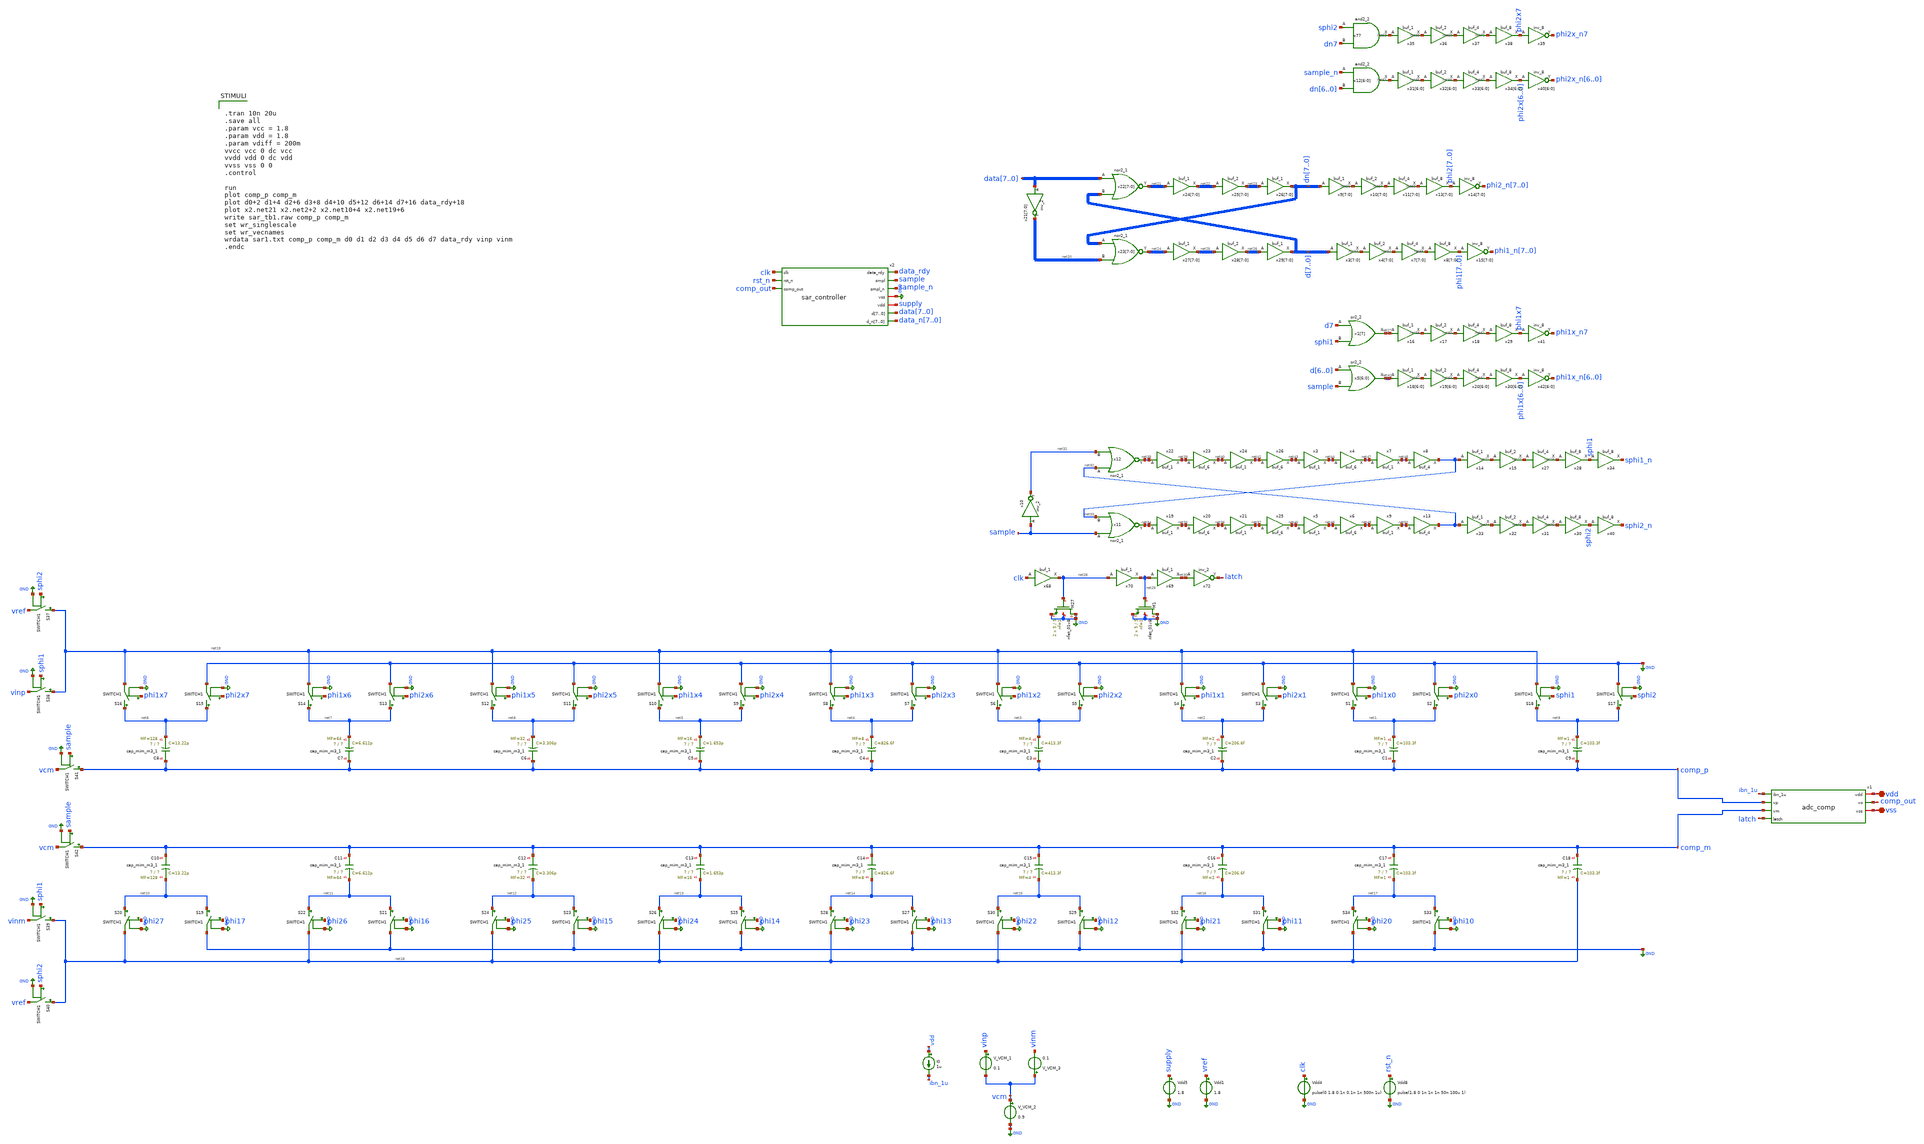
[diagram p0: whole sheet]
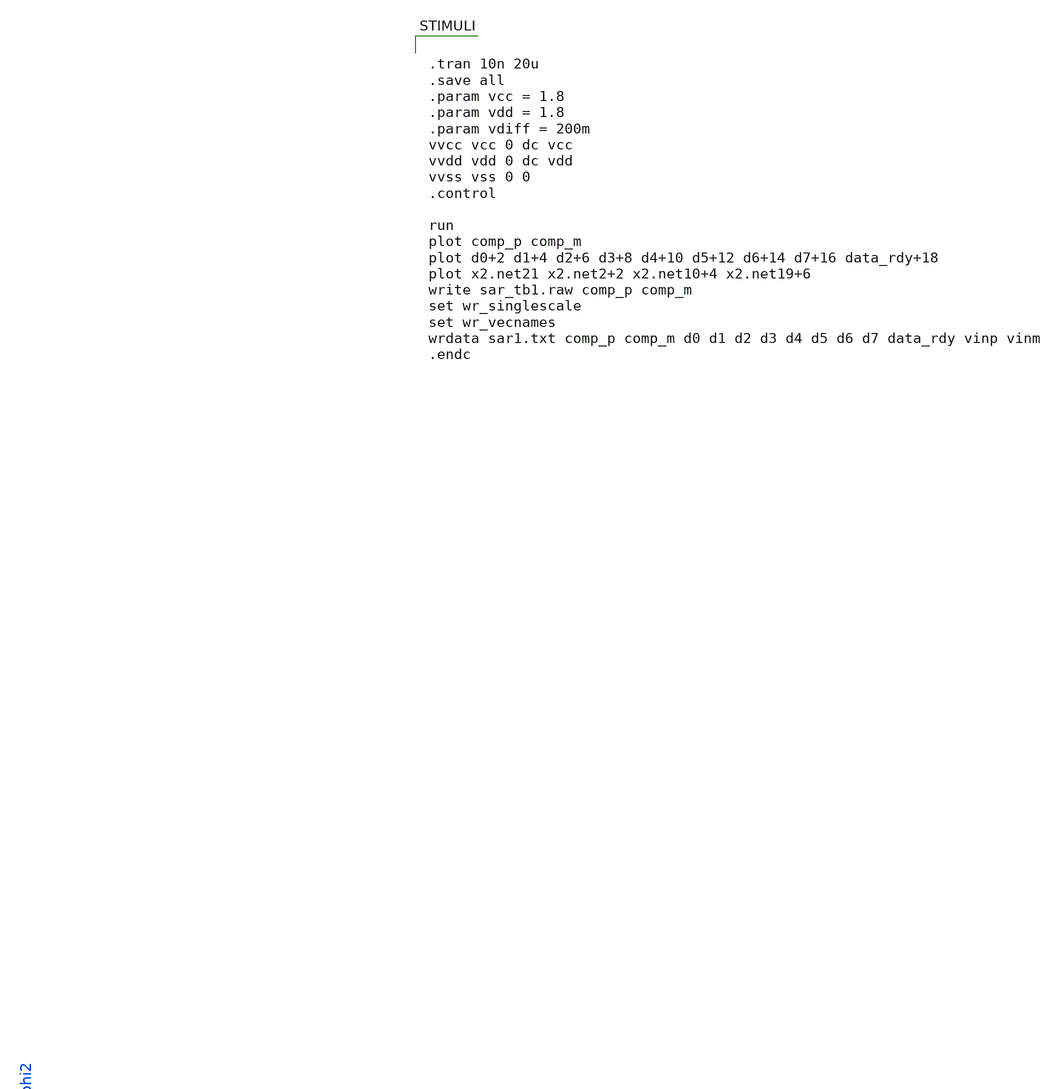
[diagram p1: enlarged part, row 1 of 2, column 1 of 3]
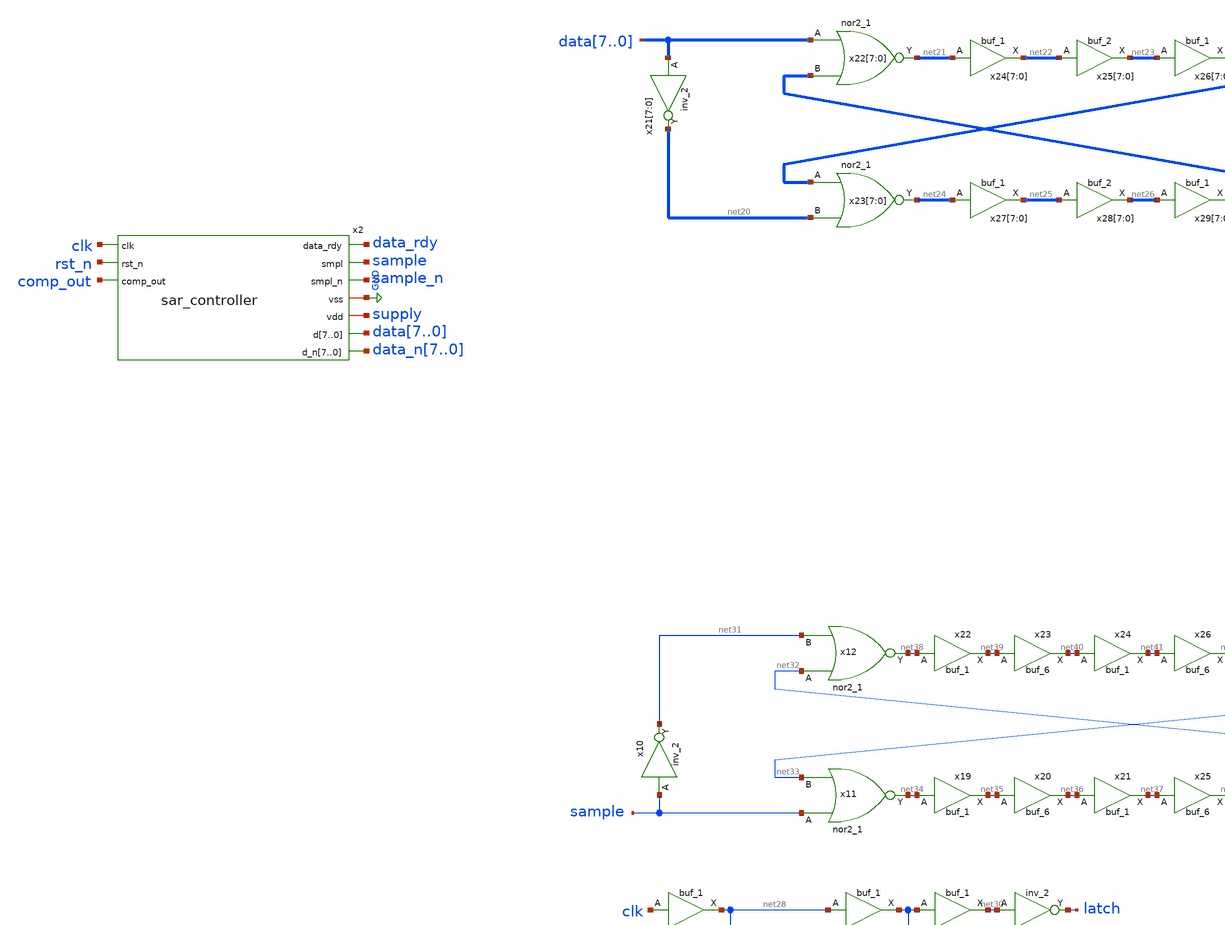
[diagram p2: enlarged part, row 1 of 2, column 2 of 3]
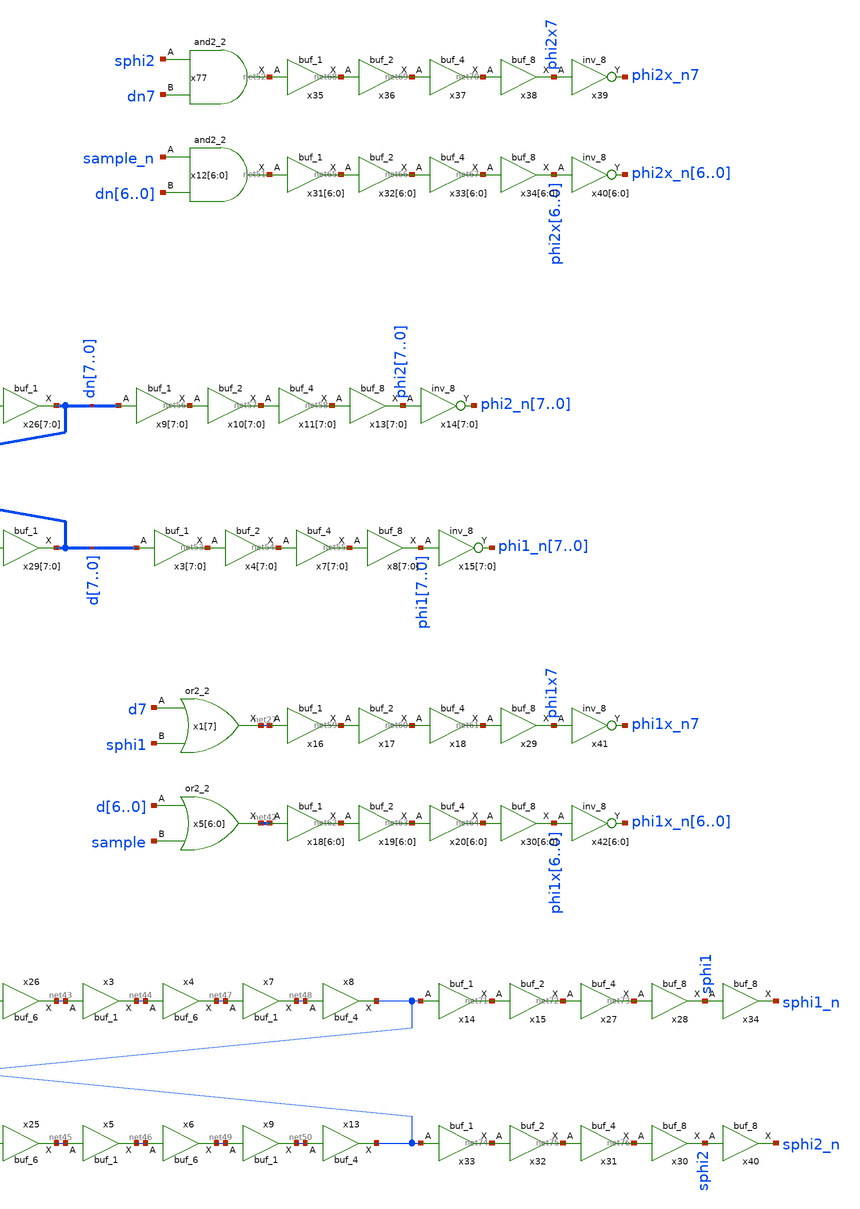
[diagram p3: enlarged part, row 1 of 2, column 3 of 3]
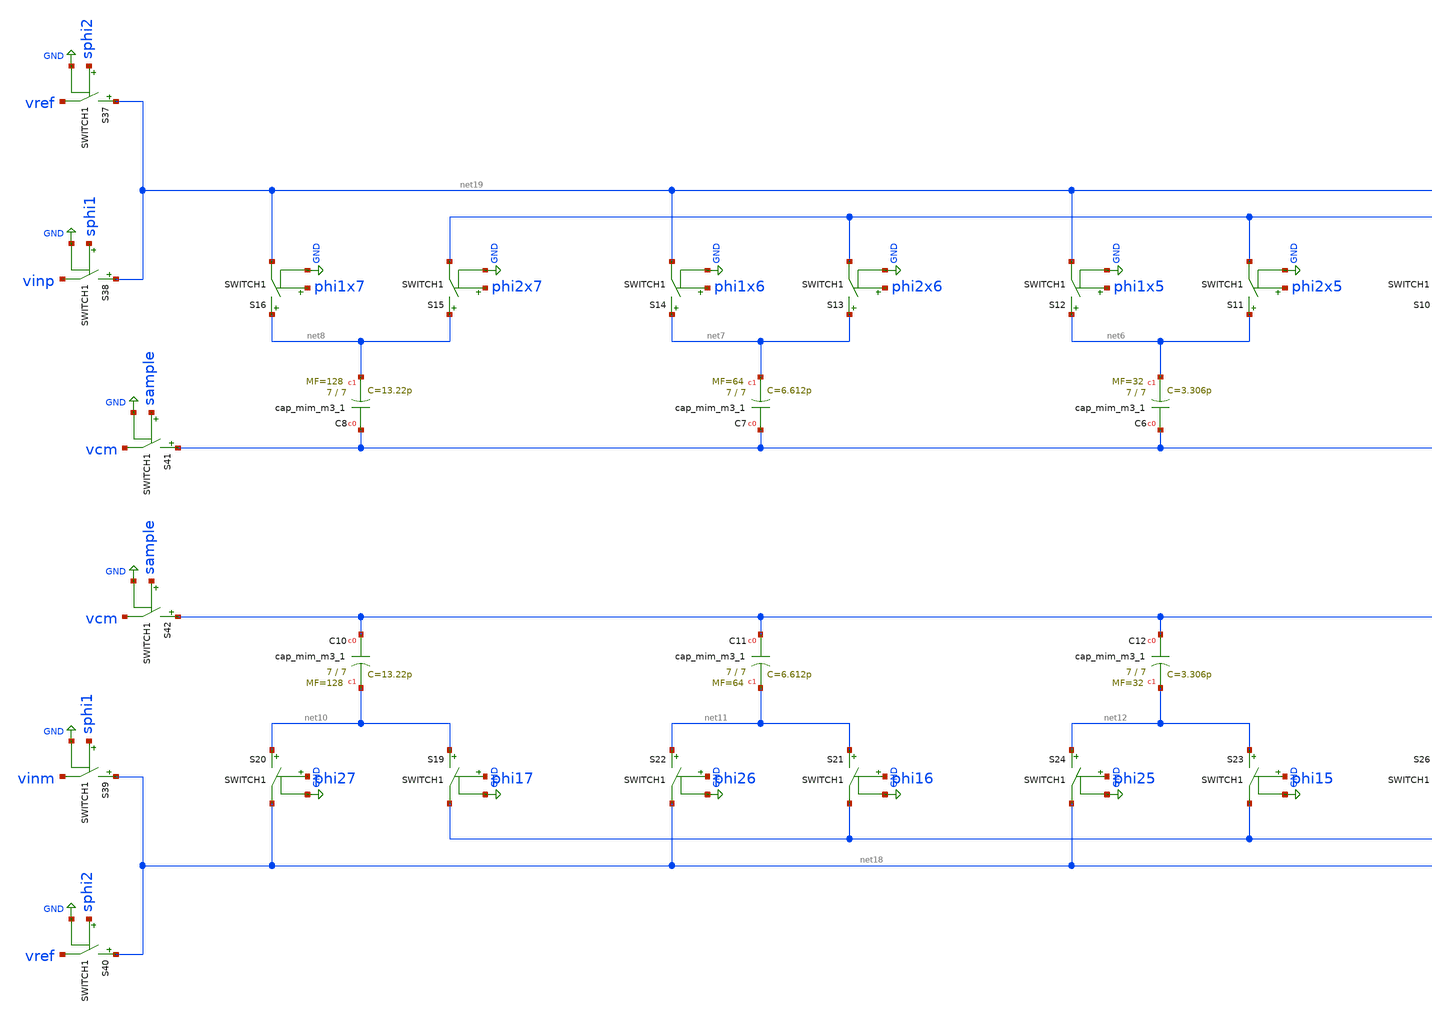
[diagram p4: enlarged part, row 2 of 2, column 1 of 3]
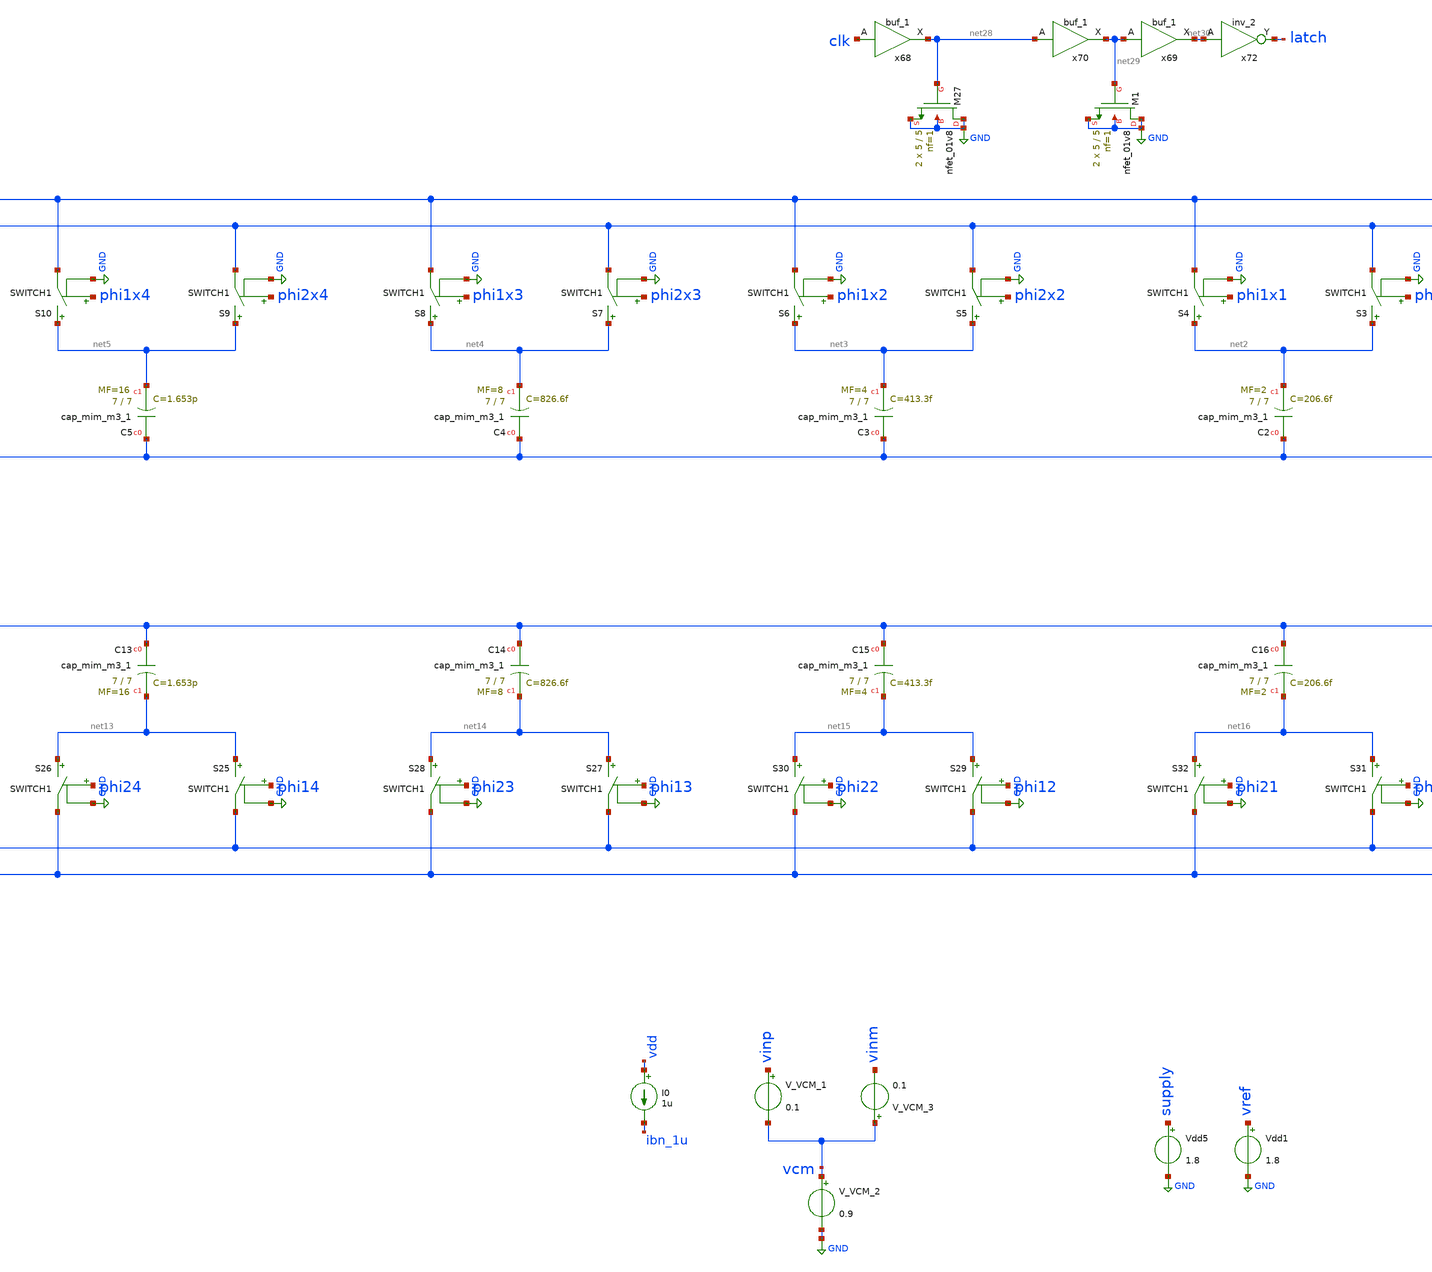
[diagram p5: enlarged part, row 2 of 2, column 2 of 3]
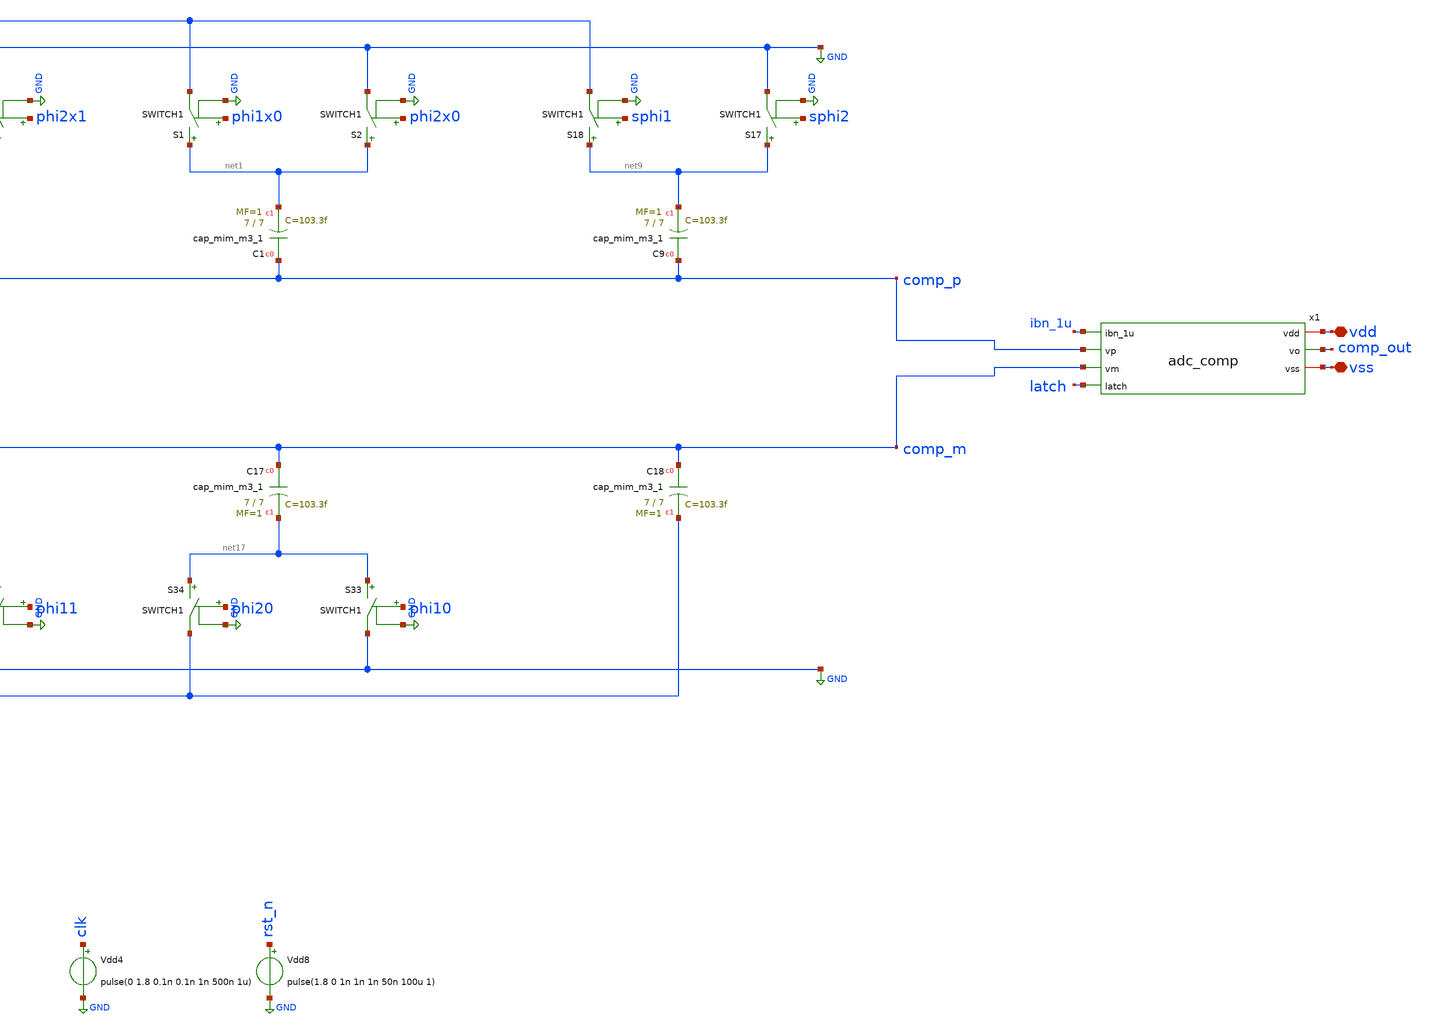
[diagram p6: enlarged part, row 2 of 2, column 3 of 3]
** sch_path: top/test/testbench/sar_tb1.sch
.lib $::SKYWATER_MODELS/sky130.lib.spice tt
.include $::SKYWATER_STDCELLS/sky130_fd_sc_hd.spice

**.subckt sar_tb1 vdd vss
*.iopin vdd
*.iopin vss
XC1 comp_p net1 sky130_fd_pr__cap_mim_m3_1 W=7 L=7 MF=1 m=1
S2 net1 GND phi2x0 GND SWITCH1
S1 net1 net19 phi1x0 GND SWITCH1
XC2 comp_p net2 sky130_fd_pr__cap_mim_m3_1 W=7 L=7 MF=2 m=2
S3 net2 GND phi2x1 GND SWITCH1
S4 net2 net19 phi1x1 GND SWITCH1
XC3 comp_p net3 sky130_fd_pr__cap_mim_m3_1 W=7 L=7 MF=4 m=4
S5 net3 GND phi2x2 GND SWITCH1
S6 net3 net19 phi1x2 GND SWITCH1
XC4 comp_p net4 sky130_fd_pr__cap_mim_m3_1 W=7 L=7 MF=8 m=8
S7 net4 GND phi2x3 GND SWITCH1
S8 net4 net19 phi1x3 GND SWITCH1
XC5 comp_p net5 sky130_fd_pr__cap_mim_m3_1 W=7 L=7 MF=16 m=16
S9 net5 GND phi2x4 GND SWITCH1
S10 net5 net19 phi1x4 GND SWITCH1
XC6 comp_p net6 sky130_fd_pr__cap_mim_m3_1 W=7 L=7 MF=32 m=32
S11 net6 GND phi2x5 GND SWITCH1
S12 net6 net19 phi1x5 GND SWITCH1
XC7 comp_p net7 sky130_fd_pr__cap_mim_m3_1 W=7 L=7 MF=64 m=64
S13 net7 GND phi2x6 GND SWITCH1
S14 net7 net19 phi1x6 GND SWITCH1
S15 net8 GND phi2x7 GND SWITCH1
S16 net8 net19 phi1x7 GND SWITCH1
XC9 comp_p net9 sky130_fd_pr__cap_mim_m3_1 W=7 L=7 MF=1 m=1
S17 net9 GND sphi2 GND SWITCH1
S18 net9 net19 sphi1 GND SWITCH1
XC10 comp_m net10 sky130_fd_pr__cap_mim_m3_1 W=7 L=7 MF=128 m=128
S19 net10 GND phi17 GND SWITCH1
S20 net10 net18 phi27 GND SWITCH1
XC11 comp_m net11 sky130_fd_pr__cap_mim_m3_1 W=7 L=7 MF=64 m=64
S21 net11 GND phi16 GND SWITCH1
S22 net11 net18 phi26 GND SWITCH1
XC12 comp_m net12 sky130_fd_pr__cap_mim_m3_1 W=7 L=7 MF=32 m=32
S23 net12 GND phi15 GND SWITCH1
S24 net12 net18 phi25 GND SWITCH1
XC13 comp_m net13 sky130_fd_pr__cap_mim_m3_1 W=7 L=7 MF=16 m=16
S25 net13 GND phi14 GND SWITCH1
S26 net13 net18 phi24 GND SWITCH1
XC14 comp_m net14 sky130_fd_pr__cap_mim_m3_1 W=7 L=7 MF=8 m=8
S27 net14 GND phi13 GND SWITCH1
S28 net14 net18 phi23 GND SWITCH1
XC15 comp_m net15 sky130_fd_pr__cap_mim_m3_1 W=7 L=7 MF=4 m=4
S29 net15 GND phi12 GND SWITCH1
S30 net15 net18 phi22 GND SWITCH1
XC16 comp_m net16 sky130_fd_pr__cap_mim_m3_1 W=7 L=7 MF=2 m=2
S31 net16 GND phi11 GND SWITCH1
S32 net16 net18 phi21 GND SWITCH1
XC17 comp_m net17 sky130_fd_pr__cap_mim_m3_1 W=7 L=7 MF=1 m=1
S33 net17 GND phi10 GND SWITCH1
S34 net17 net18 phi20 GND SWITCH1
XC18 comp_m net18 sky130_fd_pr__cap_mim_m3_1 W=7 L=7 MF=1 m=1
S37 net19 vref sphi2 GND SWITCH1
S39 net18 vinm sphi1 GND SWITCH1
S40 net18 vref sphi2 GND SWITCH1
S41 comp_p vcm sample GND SWITCH1
S42 comp_m vcm sample GND SWITCH1
Vdd8 rst_n GND pulse(1.8 0 1n 1n 1n 50n 100u 1)
Vdd4 clk GND pulse(0 1.8 0.1n 0.1n 1n 500n 1u)
Vdd1 vref GND 1.8
S38 net19 vinp sphi1 GND SWITCH1
XC8 comp_p net8 sky130_fd_pr__cap_mim_m3_1 W=7 L=7 MF=128 m=128
x2 clk data_rdy sample rst_n sample_n comp_out GND supply data7 data6 data5 data4 data3 data2 data1
+ data0 data_n7 data_n6 data_n5 data_n4 data_n3 data_n2 data_n1 data_n0 sar_controller
Vdd5 supply GND 1.8
V_VCM_2 vcm GND 0.9
V_VCM_1 vinp vcm 0.1
V_VCM_3 vcm vinm 0.1
x21[7] data7 vss vss vcc vcc net20[7] sky130_fd_sc_hd__inv_2
x21[6] data6 vss vss vcc vcc net20[6] sky130_fd_sc_hd__inv_2
x21[5] data5 vss vss vcc vcc net20[5] sky130_fd_sc_hd__inv_2
x21[4] data4 vss vss vcc vcc net20[4] sky130_fd_sc_hd__inv_2
x21[3] data3 vss vss vcc vcc net20[3] sky130_fd_sc_hd__inv_2
x21[2] data2 vss vss vcc vcc net20[2] sky130_fd_sc_hd__inv_2
x21[1] data1 vss vss vcc vcc net20[1] sky130_fd_sc_hd__inv_2
x21[0] data0 vss vss vcc vcc net20[0] sky130_fd_sc_hd__inv_2
x22[7] data7 d7 vss vss vdd vdd net21[7] sky130_fd_sc_hd__nor2_1
x22[6] data6 d6 vss vss vdd vdd net21[6] sky130_fd_sc_hd__nor2_1
x22[5] data5 d5 vss vss vdd vdd net21[5] sky130_fd_sc_hd__nor2_1
x22[4] data4 d4 vss vss vdd vdd net21[4] sky130_fd_sc_hd__nor2_1
x22[3] data3 d3 vss vss vdd vdd net21[3] sky130_fd_sc_hd__nor2_1
x22[2] data2 d2 vss vss vdd vdd net21[2] sky130_fd_sc_hd__nor2_1
x22[1] data1 d1 vss vss vdd vdd net21[1] sky130_fd_sc_hd__nor2_1
x22[0] data0 d0 vss vss vdd vdd net21[0] sky130_fd_sc_hd__nor2_1
x23[7] dn7 net20[7] vss vss vdd vdd net24[7] sky130_fd_sc_hd__nor2_1
x23[6] dn6 net20[6] vss vss vdd vdd net24[6] sky130_fd_sc_hd__nor2_1
x23[5] dn5 net20[5] vss vss vdd vdd net24[5] sky130_fd_sc_hd__nor2_1
x23[4] dn4 net20[4] vss vss vdd vdd net24[4] sky130_fd_sc_hd__nor2_1
x23[3] dn3 net20[3] vss vss vdd vdd net24[3] sky130_fd_sc_hd__nor2_1
x23[2] dn2 net20[2] vss vss vdd vdd net24[2] sky130_fd_sc_hd__nor2_1
x23[1] dn1 net20[1] vss vss vdd vdd net24[1] sky130_fd_sc_hd__nor2_1
x23[0] dn0 net20[0] vss vss vdd vdd net24[0] sky130_fd_sc_hd__nor2_1
x24[7] net21[7] vss vss vdd vdd net22[7] sky130_fd_sc_hd__buf_1
x24[6] net21[6] vss vss vdd vdd net22[6] sky130_fd_sc_hd__buf_1
x24[5] net21[5] vss vss vdd vdd net22[5] sky130_fd_sc_hd__buf_1
x24[4] net21[4] vss vss vdd vdd net22[4] sky130_fd_sc_hd__buf_1
x24[3] net21[3] vss vss vdd vdd net22[3] sky130_fd_sc_hd__buf_1
x24[2] net21[2] vss vss vdd vdd net22[2] sky130_fd_sc_hd__buf_1
x24[1] net21[1] vss vss vdd vdd net22[1] sky130_fd_sc_hd__buf_1
x24[0] net21[0] vss vss vdd vdd net22[0] sky130_fd_sc_hd__buf_1
x25[7] net22[7] vss vss vdd vdd net23[7] sky130_fd_sc_hd__buf_2
x25[6] net22[6] vss vss vdd vdd net23[6] sky130_fd_sc_hd__buf_2
x25[5] net22[5] vss vss vdd vdd net23[5] sky130_fd_sc_hd__buf_2
x25[4] net22[4] vss vss vdd vdd net23[4] sky130_fd_sc_hd__buf_2
x25[3] net22[3] vss vss vdd vdd net23[3] sky130_fd_sc_hd__buf_2
x25[2] net22[2] vss vss vdd vdd net23[2] sky130_fd_sc_hd__buf_2
x25[1] net22[1] vss vss vdd vdd net23[1] sky130_fd_sc_hd__buf_2
x25[0] net22[0] vss vss vdd vdd net23[0] sky130_fd_sc_hd__buf_2
x26[7] net23[7] vss vss vdd vdd dn7 sky130_fd_sc_hd__buf_1
x26[6] net23[6] vss vss vdd vdd dn6 sky130_fd_sc_hd__buf_1
x26[5] net23[5] vss vss vdd vdd dn5 sky130_fd_sc_hd__buf_1
x26[4] net23[4] vss vss vdd vdd dn4 sky130_fd_sc_hd__buf_1
x26[3] net23[3] vss vss vdd vdd dn3 sky130_fd_sc_hd__buf_1
x26[2] net23[2] vss vss vdd vdd dn2 sky130_fd_sc_hd__buf_1
x26[1] net23[1] vss vss vdd vdd dn1 sky130_fd_sc_hd__buf_1
x26[0] net23[0] vss vss vdd vdd dn0 sky130_fd_sc_hd__buf_1
x27[7] net24[7] vss vss vdd vdd net25[7] sky130_fd_sc_hd__buf_1
x27[6] net24[6] vss vss vdd vdd net25[6] sky130_fd_sc_hd__buf_1
x27[5] net24[5] vss vss vdd vdd net25[5] sky130_fd_sc_hd__buf_1
x27[4] net24[4] vss vss vdd vdd net25[4] sky130_fd_sc_hd__buf_1
x27[3] net24[3] vss vss vdd vdd net25[3] sky130_fd_sc_hd__buf_1
x27[2] net24[2] vss vss vdd vdd net25[2] sky130_fd_sc_hd__buf_1
x27[1] net24[1] vss vss vdd vdd net25[1] sky130_fd_sc_hd__buf_1
x27[0] net24[0] vss vss vdd vdd net25[0] sky130_fd_sc_hd__buf_1
x28[7] net25[7] vss vss vdd vdd net26[7] sky130_fd_sc_hd__buf_2
x28[6] net25[6] vss vss vdd vdd net26[6] sky130_fd_sc_hd__buf_2
x28[5] net25[5] vss vss vdd vdd net26[5] sky130_fd_sc_hd__buf_2
x28[4] net25[4] vss vss vdd vdd net26[4] sky130_fd_sc_hd__buf_2
x28[3] net25[3] vss vss vdd vdd net26[3] sky130_fd_sc_hd__buf_2
x28[2] net25[2] vss vss vdd vdd net26[2] sky130_fd_sc_hd__buf_2
x28[1] net25[1] vss vss vdd vdd net26[1] sky130_fd_sc_hd__buf_2
x28[0] net25[0] vss vss vdd vdd net26[0] sky130_fd_sc_hd__buf_2
x29[7] net26[7] vss vss vdd vdd d7 sky130_fd_sc_hd__buf_1
x29[6] net26[6] vss vss vdd vdd d6 sky130_fd_sc_hd__buf_1
x29[5] net26[5] vss vss vdd vdd d5 sky130_fd_sc_hd__buf_1
x29[4] net26[4] vss vss vdd vdd d4 sky130_fd_sc_hd__buf_1
x29[3] net26[3] vss vss vdd vdd d3 sky130_fd_sc_hd__buf_1
x29[2] net26[2] vss vss vdd vdd d2 sky130_fd_sc_hd__buf_1
x29[1] net26[1] vss vss vdd vdd d1 sky130_fd_sc_hd__buf_1
x29[0] net26[0] vss vss vdd vdd d0 sky130_fd_sc_hd__buf_1
x1[7] d7 sphi1 vss vss vcc vcc net27 sky130_fd_sc_hd__or2_2
x12[6] sample_n dn6 vss vss vcc vcc net51[6] sky130_fd_sc_hd__and2_2
x12[5] sample_n dn5 vss vss vcc vcc net51[5] sky130_fd_sc_hd__and2_2
x12[4] sample_n dn4 vss vss vcc vcc net51[4] sky130_fd_sc_hd__and2_2
x12[3] sample_n dn3 vss vss vcc vcc net51[3] sky130_fd_sc_hd__and2_2
x12[2] sample_n dn2 vss vss vcc vcc net51[2] sky130_fd_sc_hd__and2_2
x12[1] sample_n dn1 vss vss vcc vcc net51[1] sky130_fd_sc_hd__and2_2
x12[0] sample_n dn0 vss vss vcc vcc net51[0] sky130_fd_sc_hd__and2_2
x1 vdd comp_out ibn_1u comp_p comp_m vss latch adc_comp
I0 vdd ibn_1u 1u
x68 clk vss vss vdd vdd net28 sky130_fd_sc_hd__buf_1
x70 net28 vss vss vdd vdd net29 sky130_fd_sc_hd__buf_1
x72 net30 vss vss vcc vcc latch sky130_fd_sc_hd__inv_2
XM27 GND net28 GND GND sky130_fd_pr__nfet_01v8 L=5 W=5 nf=1 ad='int((nf+1)/2) * W/nf * 0.29' as='int((nf+2)/2) * W/nf * 0.29'
+ pd='2*int((nf+1)/2) * (W/nf + 0.29)' ps='2*int((nf+2)/2) * (W/nf + 0.29)' nrd='0.29 / W' nrs='0.29 / W'
+ sa=0 sb=0 sd=0 mult=2 m=2
XM1 GND net29 GND GND sky130_fd_pr__nfet_01v8 L=5 W=5 nf=1 ad='int((nf+1)/2) * W/nf * 0.29' as='int((nf+2)/2) * W/nf * 0.29'
+ pd='2*int((nf+1)/2) * (W/nf + 0.29)' ps='2*int((nf+2)/2) * (W/nf + 0.29)' nrd='0.29 / W' nrs='0.29 / W'
+ sa=0 sb=0 sd=0 mult=2 m=2
x69 net29 vss vss vdd vdd net30 sky130_fd_sc_hd__buf_1
x10 sample vss vss vcc vcc net31 sky130_fd_sc_hd__inv_2
x11 sample net33 vss vss vdd vdd net34 sky130_fd_sc_hd__nor2_1
x12 net32 net31 vss vss vdd vdd net38 sky130_fd_sc_hd__nor2_1
x19 net34 vss vss vdd vdd net35 sky130_fd_sc_hd__buf_1
x20 net35 vss vss vdd vdd net36 sky130_fd_sc_hd__buf_6
x21 net36 vss vss vdd vdd net37 sky130_fd_sc_hd__buf_1
x22 net38 vss vss vdd vdd net39 sky130_fd_sc_hd__buf_1
x23 net39 vss vss vdd vdd net40 sky130_fd_sc_hd__buf_6
x24 net40 vss vss vdd vdd net41 sky130_fd_sc_hd__buf_1
x25 net37 vss vss vdd vdd net45 sky130_fd_sc_hd__buf_6
x26 net41 vss vss vdd vdd net43 sky130_fd_sc_hd__buf_6
x5[6] d6 sample vss vss vcc vcc net42[6] sky130_fd_sc_hd__or2_2
x5[5] d5 sample vss vss vcc vcc net42[5] sky130_fd_sc_hd__or2_2
x5[4] d4 sample vss vss vcc vcc net42[4] sky130_fd_sc_hd__or2_2
x5[3] d3 sample vss vss vcc vcc net42[3] sky130_fd_sc_hd__or2_2
x5[2] d2 sample vss vss vcc vcc net42[2] sky130_fd_sc_hd__or2_2
x5[1] d1 sample vss vss vcc vcc net42[1] sky130_fd_sc_hd__or2_2
x5[0] d0 sample vss vss vcc vcc net42[0] sky130_fd_sc_hd__or2_2
x77 sphi2 dn7 vss vss vcc vcc net52 sky130_fd_sc_hd__and2_2
x3 net43 vss vss vdd vdd net44 sky130_fd_sc_hd__buf_1
x4 net44 vss vss vdd vdd net47 sky130_fd_sc_hd__buf_6
x5 net45 vss vss vdd vdd net46 sky130_fd_sc_hd__buf_1
x6 net46 vss vss vdd vdd net49 sky130_fd_sc_hd__buf_6
x7 net47 vss vss vdd vdd net48 sky130_fd_sc_hd__buf_1
x8 net48 vss vss vdd vdd net33 sky130_fd_sc_hd__buf_4
x9 net49 vss vss vdd vdd net50 sky130_fd_sc_hd__buf_1
x13 net50 vss vss vdd vdd net32 sky130_fd_sc_hd__buf_4
x3[7] d7 vss vss vdd vdd net53[7] sky130_fd_sc_hd__buf_1
x3[6] d6 vss vss vdd vdd net53[6] sky130_fd_sc_hd__buf_1
x3[5] d5 vss vss vdd vdd net53[5] sky130_fd_sc_hd__buf_1
x3[4] d4 vss vss vdd vdd net53[4] sky130_fd_sc_hd__buf_1
x3[3] d3 vss vss vdd vdd net53[3] sky130_fd_sc_hd__buf_1
x3[2] d2 vss vss vdd vdd net53[2] sky130_fd_sc_hd__buf_1
x3[1] d1 vss vss vdd vdd net53[1] sky130_fd_sc_hd__buf_1
x3[0] d0 vss vss vdd vdd net53[0] sky130_fd_sc_hd__buf_1
x4[7] net53[7] vss vss vdd vdd net54[7] sky130_fd_sc_hd__buf_2
x4[6] net53[6] vss vss vdd vdd net54[6] sky130_fd_sc_hd__buf_2
x4[5] net53[5] vss vss vdd vdd net54[5] sky130_fd_sc_hd__buf_2
x4[4] net53[4] vss vss vdd vdd net54[4] sky130_fd_sc_hd__buf_2
x4[3] net53[3] vss vss vdd vdd net54[3] sky130_fd_sc_hd__buf_2
x4[2] net53[2] vss vss vdd vdd net54[2] sky130_fd_sc_hd__buf_2
x4[1] net53[1] vss vss vdd vdd net54[1] sky130_fd_sc_hd__buf_2
x4[0] net53[0] vss vss vdd vdd net54[0] sky130_fd_sc_hd__buf_2
x7[7] net54[7] vss vss vdd vdd net55[7] sky130_fd_sc_hd__buf_4
x7[6] net54[6] vss vss vdd vdd net55[6] sky130_fd_sc_hd__buf_4
x7[5] net54[5] vss vss vdd vdd net55[5] sky130_fd_sc_hd__buf_4
x7[4] net54[4] vss vss vdd vdd net55[4] sky130_fd_sc_hd__buf_4
x7[3] net54[3] vss vss vdd vdd net55[3] sky130_fd_sc_hd__buf_4
x7[2] net54[2] vss vss vdd vdd net55[2] sky130_fd_sc_hd__buf_4
x7[1] net54[1] vss vss vdd vdd net55[1] sky130_fd_sc_hd__buf_4
x7[0] net54[0] vss vss vdd vdd net55[0] sky130_fd_sc_hd__buf_4
x8[7] net55[7] vss vss vdd vdd phi17 sky130_fd_sc_hd__buf_8
x8[6] net55[6] vss vss vdd vdd phi16 sky130_fd_sc_hd__buf_8
x8[5] net55[5] vss vss vdd vdd phi15 sky130_fd_sc_hd__buf_8
x8[4] net55[4] vss vss vdd vdd phi14 sky130_fd_sc_hd__buf_8
x8[3] net55[3] vss vss vdd vdd phi13 sky130_fd_sc_hd__buf_8
x8[2] net55[2] vss vss vdd vdd phi12 sky130_fd_sc_hd__buf_8
x8[1] net55[1] vss vss vdd vdd phi11 sky130_fd_sc_hd__buf_8
x8[0] net55[0] vss vss vdd vdd phi10 sky130_fd_sc_hd__buf_8
x9[7] dn7 vss vss vdd vdd net56[7] sky130_fd_sc_hd__buf_1
x9[6] dn6 vss vss vdd vdd net56[6] sky130_fd_sc_hd__buf_1
x9[5] dn5 vss vss vdd vdd net56[5] sky130_fd_sc_hd__buf_1
x9[4] dn4 vss vss vdd vdd net56[4] sky130_fd_sc_hd__buf_1
x9[3] dn3 vss vss vdd vdd net56[3] sky130_fd_sc_hd__buf_1
x9[2] dn2 vss vss vdd vdd net56[2] sky130_fd_sc_hd__buf_1
x9[1] dn1 vss vss vdd vdd net56[1] sky130_fd_sc_hd__buf_1
x9[0] dn0 vss vss vdd vdd net56[0] sky130_fd_sc_hd__buf_1
x10[7] net56[7] vss vss vdd vdd net57[7] sky130_fd_sc_hd__buf_2
x10[6] net56[6] vss vss vdd vdd net57[6] sky130_fd_sc_hd__buf_2
x10[5] net56[5] vss vss vdd vdd net57[5] sky130_fd_sc_hd__buf_2
x10[4] net56[4] vss vss vdd vdd net57[4] sky130_fd_sc_hd__buf_2
x10[3] net56[3] vss vss vdd vdd net57[3] sky130_fd_sc_hd__buf_2
x10[2] net56[2] vss vss vdd vdd net57[2] sky130_fd_sc_hd__buf_2
x10[1] net56[1] vss vss vdd vdd net57[1] sky130_fd_sc_hd__buf_2
x10[0] net56[0] vss vss vdd vdd net57[0] sky130_fd_sc_hd__buf_2
x11[7] net57[7] vss vss vdd vdd net58[7] sky130_fd_sc_hd__buf_4
x11[6] net57[6] vss vss vdd vdd net58[6] sky130_fd_sc_hd__buf_4
x11[5] net57[5] vss vss vdd vdd net58[5] sky130_fd_sc_hd__buf_4
x11[4] net57[4] vss vss vdd vdd net58[4] sky130_fd_sc_hd__buf_4
x11[3] net57[3] vss vss vdd vdd net58[3] sky130_fd_sc_hd__buf_4
x11[2] net57[2] vss vss vdd vdd net58[2] sky130_fd_sc_hd__buf_4
x11[1] net57[1] vss vss vdd vdd net58[1] sky130_fd_sc_hd__buf_4
x11[0] net57[0] vss vss vdd vdd net58[0] sky130_fd_sc_hd__buf_4
x13[7] net58[7] vss vss vdd vdd phi27 sky130_fd_sc_hd__buf_8
x13[6] net58[6] vss vss vdd vdd phi26 sky130_fd_sc_hd__buf_8
x13[5] net58[5] vss vss vdd vdd phi25 sky130_fd_sc_hd__buf_8
x13[4] net58[4] vss vss vdd vdd phi24 sky130_fd_sc_hd__buf_8
x13[3] net58[3] vss vss vdd vdd phi23 sky130_fd_sc_hd__buf_8
x13[2] net58[2] vss vss vdd vdd phi22 sky130_fd_sc_hd__buf_8
x13[1] net58[1] vss vss vdd vdd phi21 sky130_fd_sc_hd__buf_8
x13[0] net58[0] vss vss vdd vdd phi20 sky130_fd_sc_hd__buf_8
x14[7] phi27 vss vss vdd vdd phi2_n7 sky130_fd_sc_hd__inv_8
x14[6] phi26 vss vss vdd vdd phi2_n6 sky130_fd_sc_hd__inv_8
x14[5] phi25 vss vss vdd vdd phi2_n5 sky130_fd_sc_hd__inv_8
x14[4] phi24 vss vss vdd vdd phi2_n4 sky130_fd_sc_hd__inv_8
x14[3] phi23 vss vss vdd vdd phi2_n3 sky130_fd_sc_hd__inv_8
x14[2] phi22 vss vss vdd vdd phi2_n2 sky130_fd_sc_hd__inv_8
x14[1] phi21 vss vss vdd vdd phi2_n1 sky130_fd_sc_hd__inv_8
x14[0] phi20 vss vss vdd vdd phi2_n0 sky130_fd_sc_hd__inv_8
x15[7] phi17 vss vss vdd vdd phi1_n7 sky130_fd_sc_hd__inv_8
x15[6] phi16 vss vss vdd vdd phi1_n6 sky130_fd_sc_hd__inv_8
x15[5] phi15 vss vss vdd vdd phi1_n5 sky130_fd_sc_hd__inv_8
x15[4] phi14 vss vss vdd vdd phi1_n4 sky130_fd_sc_hd__inv_8
x15[3] phi13 vss vss vdd vdd phi1_n3 sky130_fd_sc_hd__inv_8
x15[2] phi12 vss vss vdd vdd phi1_n2 sky130_fd_sc_hd__inv_8
x15[1] phi11 vss vss vdd vdd phi1_n1 sky130_fd_sc_hd__inv_8
x15[0] phi10 vss vss vdd vdd phi1_n0 sky130_fd_sc_hd__inv_8
x16 net27 vss vss vdd vdd net59 sky130_fd_sc_hd__buf_1
x17 net59 vss vss vdd vdd net60 sky130_fd_sc_hd__buf_2
x18 net60 vss vss vdd vdd net61 sky130_fd_sc_hd__buf_4
x29 net61 vss vss vdd vdd phi1x7 sky130_fd_sc_hd__buf_8
x18[6] net42[6] vss vss vdd vdd net62[6] sky130_fd_sc_hd__buf_1
x18[5] net42[5] vss vss vdd vdd net62[5] sky130_fd_sc_hd__buf_1
x18[4] net42[4] vss vss vdd vdd net62[4] sky130_fd_sc_hd__buf_1
x18[3] net42[3] vss vss vdd vdd net62[3] sky130_fd_sc_hd__buf_1
x18[2] net42[2] vss vss vdd vdd net62[2] sky130_fd_sc_hd__buf_1
x18[1] net42[1] vss vss vdd vdd net62[1] sky130_fd_sc_hd__buf_1
x18[0] net42[0] vss vss vdd vdd net62[0] sky130_fd_sc_hd__buf_1
x19[6] net62[6] vss vss vdd vdd net63[6] sky130_fd_sc_hd__buf_2
x19[5] net62[5] vss vss vdd vdd net63[5] sky130_fd_sc_hd__buf_2
x19[4] net62[4] vss vss vdd vdd net63[4] sky130_fd_sc_hd__buf_2
x19[3] net62[3] vss vss vdd vdd net63[3] sky130_fd_sc_hd__buf_2
x19[2] net62[2] vss vss vdd vdd net63[2] sky130_fd_sc_hd__buf_2
x19[1] net62[1] vss vss vdd vdd net63[1] sky130_fd_sc_hd__buf_2
x19[0] net62[0] vss vss vdd vdd net63[0] sky130_fd_sc_hd__buf_2
x20[6] net63[6] vss vss vdd vdd net64[6] sky130_fd_sc_hd__buf_4
x20[5] net63[5] vss vss vdd vdd net64[5] sky130_fd_sc_hd__buf_4
x20[4] net63[4] vss vss vdd vdd net64[4] sky130_fd_sc_hd__buf_4
x20[3] net63[3] vss vss vdd vdd net64[3] sky130_fd_sc_hd__buf_4
x20[2] net63[2] vss vss vdd vdd net64[2] sky130_fd_sc_hd__buf_4
x20[1] net63[1] vss vss vdd vdd net64[1] sky130_fd_sc_hd__buf_4
x20[0] net63[0] vss vss vdd vdd net64[0] sky130_fd_sc_hd__buf_4
x30[6] net64[6] vss vss vdd vdd phi1x6 sky130_fd_sc_hd__buf_8
x30[5] net64[5] vss vss vdd vdd phi1x5 sky130_fd_sc_hd__buf_8
x30[4] net64[4] vss vss vdd vdd phi1x4 sky130_fd_sc_hd__buf_8
x30[3] net64[3] vss vss vdd vdd phi1x3 sky130_fd_sc_hd__buf_8
x30[2] net64[2] vss vss vdd vdd phi1x2 sky130_fd_sc_hd__buf_8
x30[1] net64[1] vss vss vdd vdd phi1x1 sky130_fd_sc_hd__buf_8
x30[0] net64[0] vss vss vdd vdd phi1x0 sky130_fd_sc_hd__buf_8
x31[6] net51[6] vss vss vdd vdd net65[6] sky130_fd_sc_hd__buf_1
x31[5] net51[5] vss vss vdd vdd net65[5] sky130_fd_sc_hd__buf_1
x31[4] net51[4] vss vss vdd vdd net65[4] sky130_fd_sc_hd__buf_1
x31[3] net51[3] vss vss vdd vdd net65[3] sky130_fd_sc_hd__buf_1
x31[2] net51[2] vss vss vdd vdd net65[2] sky130_fd_sc_hd__buf_1
x31[1] net51[1] vss vss vdd vdd net65[1] sky130_fd_sc_hd__buf_1
x31[0] net51[0] vss vss vdd vdd net65[0] sky130_fd_sc_hd__buf_1
x32[6] net65[6] vss vss vdd vdd net66[6] sky130_fd_sc_hd__buf_2
x32[5] net65[5] vss vss vdd vdd net66[5] sky130_fd_sc_hd__buf_2
x32[4] net65[4] vss vss vdd vdd net66[4] sky130_fd_sc_hd__buf_2
x32[3] net65[3] vss vss vdd vdd net66[3] sky130_fd_sc_hd__buf_2
x32[2] net65[2] vss vss vdd vdd net66[2] sky130_fd_sc_hd__buf_2
x32[1] net65[1] vss vss vdd vdd net66[1] sky130_fd_sc_hd__buf_2
x32[0] net65[0] vss vss vdd vdd net66[0] sky130_fd_sc_hd__buf_2
x33[6] net66[6] vss vss vdd vdd net67[6] sky130_fd_sc_hd__buf_4
x33[5] net66[5] vss vss vdd vdd net67[5] sky130_fd_sc_hd__buf_4
x33[4] net66[4] vss vss vdd vdd net67[4] sky130_fd_sc_hd__buf_4
x33[3] net66[3] vss vss vdd vdd net67[3] sky130_fd_sc_hd__buf_4
x33[2] net66[2] vss vss vdd vdd net67[2] sky130_fd_sc_hd__buf_4
x33[1] net66[1] vss vss vdd vdd net67[1] sky130_fd_sc_hd__buf_4
x33[0] net66[0] vss vss vdd vdd net67[0] sky130_fd_sc_hd__buf_4
x34[6] net67[6] vss vss vdd vdd phi2x6 sky130_fd_sc_hd__buf_8
x34[5] net67[5] vss vss vdd vdd phi2x5 sky130_fd_sc_hd__buf_8
x34[4] net67[4] vss vss vdd vdd phi2x4 sky130_fd_sc_hd__buf_8
x34[3] net67[3] vss vss vdd vdd phi2x3 sky130_fd_sc_hd__buf_8
x34[2] net67[2] vss vss vdd vdd phi2x2 sky130_fd_sc_hd__buf_8
x34[1] net67[1] vss vss vdd vdd phi2x1 sky130_fd_sc_hd__buf_8
x34[0] net67[0] vss vss vdd vdd phi2x0 sky130_fd_sc_hd__buf_8
x35 net52 vss vss vdd vdd net68 sky130_fd_sc_hd__buf_1
x36 net68 vss vss vdd vdd net69 sky130_fd_sc_hd__buf_2
x37 net69 vss vss vdd vdd net70 sky130_fd_sc_hd__buf_4
x38 net70 vss vss vdd vdd phi2x7 sky130_fd_sc_hd__buf_8
x39 phi2x7 vss vss vdd vdd phi2x_n7 sky130_fd_sc_hd__inv_8
x40[6] phi2x6 vss vss vdd vdd phi2x_n6 sky130_fd_sc_hd__inv_8
x40[5] phi2x5 vss vss vdd vdd phi2x_n5 sky130_fd_sc_hd__inv_8
x40[4] phi2x4 vss vss vdd vdd phi2x_n4 sky130_fd_sc_hd__inv_8
x40[3] phi2x3 vss vss vdd vdd phi2x_n3 sky130_fd_sc_hd__inv_8
x40[2] phi2x2 vss vss vdd vdd phi2x_n2 sky130_fd_sc_hd__inv_8
x40[1] phi2x1 vss vss vdd vdd phi2x_n1 sky130_fd_sc_hd__inv_8
x40[0] phi2x0 vss vss vdd vdd phi2x_n0 sky130_fd_sc_hd__inv_8
x41 phi1x7 vss vss vdd vdd phi1x_n7 sky130_fd_sc_hd__inv_8
x42[6] phi1x6 vss vss vdd vdd phi1x_n6 sky130_fd_sc_hd__inv_8
x42[5] phi1x5 vss vss vdd vdd phi1x_n5 sky130_fd_sc_hd__inv_8
x42[4] phi1x4 vss vss vdd vdd phi1x_n4 sky130_fd_sc_hd__inv_8
x42[3] phi1x3 vss vss vdd vdd phi1x_n3 sky130_fd_sc_hd__inv_8
x42[2] phi1x2 vss vss vdd vdd phi1x_n2 sky130_fd_sc_hd__inv_8
x42[1] phi1x1 vss vss vdd vdd phi1x_n1 sky130_fd_sc_hd__inv_8
x42[0] phi1x0 vss vss vdd vdd phi1x_n0 sky130_fd_sc_hd__inv_8
x14 net33 vss vss vdd vdd net71 sky130_fd_sc_hd__buf_1
x15 net71 vss vss vdd vdd net72 sky130_fd_sc_hd__buf_2
x27 net72 vss vss vdd vdd net73 sky130_fd_sc_hd__buf_4
x28 net73 vss vss vdd vdd sphi1 sky130_fd_sc_hd__buf_8
x33 net32 vss vss vdd vdd net74 sky130_fd_sc_hd__buf_1
x32 net74 vss vss vdd vdd net75 sky130_fd_sc_hd__buf_2
x31 net75 vss vss vdd vdd net76 sky130_fd_sc_hd__buf_4
x30 net76 vss vss vdd vdd sphi2 sky130_fd_sc_hd__buf_8
x34 sphi1 vss vss vdd vdd sphi1_n sky130_fd_sc_hd__buf_8
x40 sphi2 vss vss vdd vdd sphi2_n sky130_fd_sc_hd__buf_8
**** begin user architecture code


.tran 10n 20u
.save all
.param vcc = 1.8
.param vdd = 1.8
.param vdiff = 200m
vvcc vcc 0 dc vcc
vvdd vdd 0 dc vdd
vvss vss 0 0
.control

run
plot comp_p comp_m
plot d0+2 d1+4 d2+6 d3+8 d4+10 d5+12 d6+14 d7+16 data_rdy+18
plot x2.net21 x2.net2+2 x2.net10+4 x2.net19+6
write sar_tb1.raw comp_p comp_m
set wr_singlescale
set wr_vecnames
wrdata sar1.txt comp_p comp_m d0 d1 d2 d3 d4 d5 d6 d7 data_rdy vinp vinm
.endc



.model SWITCH1 sw vt=0.9 vh=0 ron=1 roff =100G

**** end user architecture code
**.ends

* expanding   symbol:  /foss/designs/test/design/sar_controller.sym # of pins=10
** sym_path: test/design/sar_controller.sym
** sch_path: test/design/sar_controller.sch
.subckt sar_controller clk data_rdy smpl rst_n smpl_n comp_out vss vdd d7 d6 d5 d4 d3 d2 d1 d0 d_n7
+ d_n6 d_n5 d_n4 d_n3 d_n2 d_n1 d_n0
*.ipin rst_n
*.opin data_rdy
*.ipin clk
*.opin smpl
*.ipin comp_out
*.iopin vss
*.iopin vdd
*.opin d7,d6,d5,d4,d3,d2,d1,d0
*.opin d_n7,d_n6,d_n5,d_n4,d_n3,d_n2,d_n1,d_n0
*.opin smpl_n
x26 net2 net21 net22 net9 vss vss vdd vdd net1 net25 sky130_fd_sc_hd__dfbbp_1
x5 net19 net23 net20 vss vss vdd vdd cnv_7 net9 sky130_fd_sc_hd__dfrbp_1
* noconn #net33
x24 net19 net8 net20 vss vss vdd vdd net23 net24 sky130_fd_sc_hd__dfsbp_1
x6 net24 net20 vss vss vdd vdd net22 sky130_fd_sc_hd__and2_4
x1 net19 cnv_7 net20 vss vss vdd vdd cnv_6 net12 sky130_fd_sc_hd__dfrbp_1
x2 net19 cnv_6 net20 vss vss vdd vdd cnv_5 net13 sky130_fd_sc_hd__dfrbp_1
x3 net19 cnv_5 net20 vss vss vdd vdd cnv_4 net14 sky130_fd_sc_hd__dfrbp_1
x4 net19 cnv_4 net20 vss vss vdd vdd cnv_3 net15 sky130_fd_sc_hd__dfrbp_1
x7 net19 cnv_3 net20 vss vss vdd vdd cnv_2 net16 sky130_fd_sc_hd__dfrbp_1
x8 net19 cnv_2 net20 vss vss vdd vdd cnv_1 net17 sky130_fd_sc_hd__dfrbp_1
x9 net19 cnv_1 net20 vss vss vdd vdd cnv_0 net18 sky130_fd_sc_hd__dfrbp_1
x10 net19 cnv_0 net20 vss vss vdd vdd net8 net33 sky130_fd_sc_hd__dfrbp_1
x11 vss vss net22 vss vss vdd vdd net11 net34 sky130_fd_sc_hd__dfrbp_1
x12 net10 net21 net22 net12 vss vss vdd vdd net2 net26 sky130_fd_sc_hd__dfbbp_1
x13 net3 net21 net22 net13 vss vss vdd vdd net10 net27 sky130_fd_sc_hd__dfbbp_1
x14 net4 net21 net22 net14 vss vss vdd vdd net3 net28 sky130_fd_sc_hd__dfbbp_1
x15 net5 net21 net22 net15 vss vss vdd vdd net4 net29 sky130_fd_sc_hd__dfbbp_1
x16 net6 net21 net22 net16 vss vss vdd vdd net5 net30 sky130_fd_sc_hd__dfbbp_1
x17 net7 net21 net22 net17 vss vss vdd vdd net6 net31 sky130_fd_sc_hd__dfbbp_1
x18 net11 net21 net22 net18 vss vss vdd vdd net7 net32 sky130_fd_sc_hd__dfbbp_1
* noconn #net34
x19 net1 vss vss vdd vdd d7 sky130_fd_sc_hd__buf_2
x20 net25 vss vss vdd vdd d_n7 sky130_fd_sc_hd__buf_2
x21 net2 vss vss vdd vdd d6 sky130_fd_sc_hd__buf_2
x22 net26 vss vss vdd vdd d_n6 sky130_fd_sc_hd__buf_2
x23 net10 vss vss vdd vdd d5 sky130_fd_sc_hd__buf_2
x25 net27 vss vss vdd vdd d_n5 sky130_fd_sc_hd__buf_2
x27 net3 vss vss vdd vdd d4 sky130_fd_sc_hd__buf_2
x28 net28 vss vss vdd vdd d_n4 sky130_fd_sc_hd__buf_2
x29 net4 vss vss vdd vdd d3 sky130_fd_sc_hd__buf_2
x30 net29 vss vss vdd vdd d_n3 sky130_fd_sc_hd__buf_2
x31 net5 vss vss vdd vdd d2 sky130_fd_sc_hd__buf_2
x32 net30 vss vss vdd vdd d_n2 sky130_fd_sc_hd__buf_2
x33 net6 vss vss vdd vdd d1 sky130_fd_sc_hd__buf_2
x34 net31 vss vss vdd vdd d_n1 sky130_fd_sc_hd__buf_2
x35 net7 vss vss vdd vdd d0 sky130_fd_sc_hd__buf_2
x36 net32 vss vss vdd vdd d_n0 sky130_fd_sc_hd__buf_2
x37 net23 vss vss vdd vdd smpl sky130_fd_sc_hd__buf_2
x38 net24 vss vss vdd vdd smpl_n sky130_fd_sc_hd__buf_2
x39 net8 vss vss vdd vdd data_rdy sky130_fd_sc_hd__buf_2
x40 comp_out vss vss vdd vdd net21 sky130_fd_sc_hd__buf_4
x41 rst_n vss vss vdd vdd net20 sky130_fd_sc_hd__buf_4
x42 clk vss vss vdd vdd net19 sky130_fd_sc_hd__buf_4
.ends


* expanding   symbol:  /foss/designs/test/design/adc_comp.sym # of pins=7
** sym_path: test/design/adc_comp.sym
** sch_path: test/design/adc_comp.sch
.subckt adc_comp vdd vo ibn_1u vp vm vss latch
*.iopin vss
*.iopin vdd
*.ipin vp
*.ipin vm
*.ipin latch
*.ipin ibn_1u
*.opin vo
XM3 vom1 vp vx vss sky130_fd_pr__nfet_01v8_lvt L=1 W=2 nf=1 ad='int((nf+1)/2) * W/nf * 0.29' as='int((nf+2)/2) * W/nf * 0.29'
+ pd='2*int((nf+1)/2) * (W/nf + 0.29)' ps='2*int((nf+2)/2) * (W/nf + 0.29)' nrd='0.29 / W' nrs='0.29 / W'
+ sa=0 sb=0 sd=0 mult=8 m=8
XM4 vop1 vm vx vss sky130_fd_pr__nfet_01v8_lvt L=1 W=2 nf=1 ad='int((nf+1)/2) * W/nf * 0.29' as='int((nf+2)/2) * W/nf * 0.29'
+ pd='2*int((nf+1)/2) * (W/nf + 0.29)' ps='2*int((nf+2)/2) * (W/nf + 0.29)' nrd='0.29 / W' nrs='0.29 / W'
+ sa=0 sb=0 sd=0 mult=8 m=8
XM2 vop1 vbp vdd vdd sky130_fd_pr__pfet_01v8_lvt L=5 W=5 nf=1 ad='int((nf+1)/2) * W/nf * 0.29' as='int((nf+2)/2) * W/nf * 0.29'
+ pd='2*int((nf+1)/2) * (W/nf + 0.29)' ps='2*int((nf+2)/2) * (W/nf + 0.29)' nrd='0.29 / W' nrs='0.29 / W'
+ sa=0 sb=0 sd=0 mult=5 m=5
XM1 vom1 vbp vdd vdd sky130_fd_pr__pfet_01v8_lvt L=5 W=5 nf=1 ad='int((nf+1)/2) * W/nf * 0.29' as='int((nf+2)/2) * W/nf * 0.29'
+ pd='2*int((nf+1)/2) * (W/nf + 0.29)' ps='2*int((nf+2)/2) * (W/nf + 0.29)' nrd='0.29 / W' nrs='0.29 / W'
+ sa=0 sb=0 sd=0 mult=5 m=5
XM6 ibn_1u ibn_1u vss vss sky130_fd_pr__nfet_01v8 L=20 W=3 nf=1 ad='int((nf+1)/2) * W/nf * 0.29' as='int((nf+2)/2) * W/nf * 0.29'
+ pd='2*int((nf+1)/2) * (W/nf + 0.29)' ps='2*int((nf+2)/2) * (W/nf + 0.29)' nrd='0.29 / W' nrs='0.29 / W'
+ sa=0 sb=0 sd=0 mult=2 m=2
XM5 vx ibn_1u vss vss sky130_fd_pr__nfet_01v8 L=20 W=3 nf=1 ad='int((nf+1)/2) * W/nf * 0.29' as='int((nf+2)/2) * W/nf * 0.29'
+ pd='2*int((nf+1)/2) * (W/nf + 0.29)' ps='2*int((nf+2)/2) * (W/nf + 0.29)' nrd='0.29 / W' nrs='0.29 / W'
+ sa=0 sb=0 sd=0 mult=12 m=12
XM7 vbp ibn_1u vss vss sky130_fd_pr__nfet_01v8 L=20 W=3 nf=1 ad='int((nf+1)/2) * W/nf * 0.29' as='int((nf+2)/2) * W/nf * 0.29'
+ pd='2*int((nf+1)/2) * (W/nf + 0.29)' ps='2*int((nf+2)/2) * (W/nf + 0.29)' nrd='0.29 / W' nrs='0.29 / W'
+ sa=0 sb=0 sd=0 mult=1 m=1
XM8 vbp vbp vdd vdd sky130_fd_pr__pfet_01v8_lvt L=5 W=5 nf=1 ad='int((nf+1)/2) * W/nf * 0.29' as='int((nf+2)/2) * W/nf * 0.29'
+ pd='2*int((nf+1)/2) * (W/nf + 0.29)' ps='2*int((nf+2)/2) * (W/nf + 0.29)' nrd='0.29 / W' nrs='0.29 / W'
+ sa=0 sb=0 sd=0 mult=1 m=1
XM9 vx vop1 vdd vdd sky130_fd_pr__pfet_01v8_lvt L=1 W=5 nf=1 ad='int((nf+1)/2) * W/nf * 0.29' as='int((nf+2)/2) * W/nf * 0.29'
+ pd='2*int((nf+1)/2) * (W/nf + 0.29)' ps='2*int((nf+2)/2) * (W/nf + 0.29)' nrd='0.29 / W' nrs='0.29 / W'
+ sa=0 sb=0 sd=0 mult=2 m=2
XM10 vx vom1 vdd vdd sky130_fd_pr__pfet_01v8_lvt L=1 W=5 nf=1 ad='int((nf+1)/2) * W/nf * 0.29' as='int((nf+2)/2) * W/nf * 0.29'
+ pd='2*int((nf+1)/2) * (W/nf + 0.29)' ps='2*int((nf+2)/2) * (W/nf + 0.29)' nrd='0.29 / W' nrs='0.29 / W'
+ sa=0 sb=0 sd=0 mult=2 m=2
XM11 vop2 vom2 vss vss sky130_fd_pr__nfet_01v8 L=2 W=3 nf=1 ad='int((nf+1)/2) * W/nf * 0.29' as='int((nf+2)/2) * W/nf * 0.29'
+ pd='2*int((nf+1)/2) * (W/nf + 0.29)' ps='2*int((nf+2)/2) * (W/nf + 0.29)' nrd='0.29 / W' nrs='0.29 / W'
+ sa=0 sb=0 sd=0 mult=1 m=1
XM12 vom2 vop2 vss vss sky130_fd_pr__nfet_01v8 L=2 W=3 nf=1 ad='int((nf+1)/2) * W/nf * 0.29' as='int((nf+2)/2) * W/nf * 0.29'
+ pd='2*int((nf+1)/2) * (W/nf + 0.29)' ps='2*int((nf+2)/2) * (W/nf + 0.29)' nrd='0.29 / W' nrs='0.29 / W'
+ sa=0 sb=0 sd=0 mult=1 m=1
XM13 net4 vom1 vdd vdd sky130_fd_pr__pfet_01v8_lvt L=0.4 W=5 nf=1 ad='int((nf+1)/2) * W/nf * 0.29' as='int((nf+2)/2) * W/nf * 0.29'
+ pd='2*int((nf+1)/2) * (W/nf + 0.29)' ps='2*int((nf+2)/2) * (W/nf + 0.29)' nrd='0.29 / W' nrs='0.29 / W'
+ sa=0 sb=0 sd=0 mult=1 m=1
XM14 net3 vop1 vdd vdd sky130_fd_pr__pfet_01v8_lvt L=0.4 W=5 nf=1 ad='int((nf+1)/2) * W/nf * 0.29' as='int((nf+2)/2) * W/nf * 0.29'
+ pd='2*int((nf+1)/2) * (W/nf + 0.29)' ps='2*int((nf+2)/2) * (W/nf + 0.29)' nrd='0.29 / W' nrs='0.29 / W'
+ sa=0 sb=0 sd=0 mult=1 m=1
XM17 vom2 latch_n vss vss sky130_fd_pr__nfet_01v8 L=0.15 W=0.5 nf=1 ad='int((nf+1)/2) * W/nf * 0.29'
+ as='int((nf+2)/2) * W/nf * 0.29' pd='2*int((nf+1)/2) * (W/nf + 0.29)' ps='2*int((nf+2)/2) * (W/nf + 0.29)'
+ nrd='0.29 / W' nrs='0.29 / W' sa=0 sb=0 sd=0 mult=1 m=1
XM18 vop2 latch_n vss vss sky130_fd_pr__nfet_01v8 L=0.15 W=0.5 nf=1 ad='int((nf+1)/2) * W/nf * 0.29'
+ as='int((nf+2)/2) * W/nf * 0.29' pd='2*int((nf+1)/2) * (W/nf + 0.29)' ps='2*int((nf+2)/2) * (W/nf + 0.29)'
+ nrd='0.29 / W' nrs='0.29 / W' sa=0 sb=0 sd=0 mult=1 m=1
XM19 net1 vop2 vdd vdd sky130_fd_pr__pfet_01v8 L=0.15 W=1 nf=1 ad='int((nf+1)/2) * W/nf * 0.29' as='int((nf+2)/2) * W/nf * 0.29'
+ pd='2*int((nf+1)/2) * (W/nf + 0.29)' ps='2*int((nf+2)/2) * (W/nf + 0.29)' nrd='0.29 / W' nrs='0.29 / W'
+ sa=0 sb=0 sd=0 mult=1 m=1
XM20 net1 vop2 vss vss sky130_fd_pr__nfet_01v8 L=0.15 W=0.5 nf=1 ad='int((nf+1)/2) * W/nf * 0.29' as='int((nf+2)/2) * W/nf * 0.29'
+ pd='2*int((nf+1)/2) * (W/nf + 0.29)' ps='2*int((nf+2)/2) * (W/nf + 0.29)' nrd='0.29 / W' nrs='0.29 / W'
+ sa=0 sb=0 sd=0 mult=1 m=1
XM21 vo net1 vdd vdd sky130_fd_pr__pfet_01v8 L=0.15 W=1 nf=1 ad='int((nf+1)/2) * W/nf * 0.29' as='int((nf+2)/2) * W/nf * 0.29'
+ pd='2*int((nf+1)/2) * (W/nf + 0.29)' ps='2*int((nf+2)/2) * (W/nf + 0.29)' nrd='0.29 / W' nrs='0.29 / W'
+ sa=0 sb=0 sd=0 mult=2 m=2
XM22 vo net1 vss vss sky130_fd_pr__nfet_01v8 L=0.15 W=0.5 nf=1 ad='int((nf+1)/2) * W/nf * 0.29' as='int((nf+2)/2) * W/nf * 0.29'
+ pd='2*int((nf+1)/2) * (W/nf + 0.29)' ps='2*int((nf+2)/2) * (W/nf + 0.29)' nrd='0.29 / W' nrs='0.29 / W'
+ sa=0 sb=0 sd=0 mult=2 m=2
XM23 net2 vom2 vdd vdd sky130_fd_pr__pfet_01v8 L=0.15 W=1 nf=1 ad='int((nf+1)/2) * W/nf * 0.29' as='int((nf+2)/2) * W/nf * 0.29'
+ pd='2*int((nf+1)/2) * (W/nf + 0.29)' ps='2*int((nf+2)/2) * (W/nf + 0.29)' nrd='0.29 / W' nrs='0.29 / W'
+ sa=0 sb=0 sd=0 mult=1 m=1
XM24 net2 vom2 vss vss sky130_fd_pr__nfet_01v8 L=0.15 W=0.5 nf=1 ad='int((nf+1)/2) * W/nf * 0.29' as='int((nf+2)/2) * W/nf * 0.29'
+ pd='2*int((nf+1)/2) * (W/nf + 0.29)' ps='2*int((nf+2)/2) * (W/nf + 0.29)' nrd='0.29 / W' nrs='0.29 / W'
+ sa=0 sb=0 sd=0 mult=1 m=1
XM15 net5 vop2 net3 vdd sky130_fd_pr__pfet_01v8_lvt L=0.4 W=5 nf=1 ad='int((nf+1)/2) * W/nf * 0.29' as='int((nf+2)/2) * W/nf * 0.29'
+ pd='2*int((nf+1)/2) * (W/nf + 0.29)' ps='2*int((nf+2)/2) * (W/nf + 0.29)' nrd='0.29 / W' nrs='0.29 / W'
+ sa=0 sb=0 sd=0 mult=1 m=1
XM16 net6 vom2 net4 vdd sky130_fd_pr__pfet_01v8_lvt L=0.4 W=5 nf=1 ad='int((nf+1)/2) * W/nf * 0.29' as='int((nf+2)/2) * W/nf * 0.29'
+ pd='2*int((nf+1)/2) * (W/nf + 0.29)' ps='2*int((nf+2)/2) * (W/nf + 0.29)' nrd='0.29 / W' nrs='0.29 / W'
+ sa=0 sb=0 sd=0 mult=1 m=1
XM25 net5 latch vom2 vss sky130_fd_pr__nfet_01v8_lvt L=0.15 W=1 nf=1 ad='int((nf+1)/2) * W/nf * 0.29'
+ as='int((nf+2)/2) * W/nf * 0.29' pd='2*int((nf+1)/2) * (W/nf + 0.29)' ps='2*int((nf+2)/2) * (W/nf + 0.29)'
+ nrd='0.29 / W' nrs='0.29 / W' sa=0 sb=0 sd=0 mult=1 m=1
XM26 net6 latch vop2 vss sky130_fd_pr__nfet_01v8_lvt L=0.15 W=1 nf=1 ad='int((nf+1)/2) * W/nf * 0.29'
+ as='int((nf+2)/2) * W/nf * 0.29' pd='2*int((nf+1)/2) * (W/nf + 0.29)' ps='2*int((nf+2)/2) * (W/nf + 0.29)'
+ nrd='0.29 / W' nrs='0.29 / W' sa=0 sb=0 sd=0 mult=1 m=1
x30 latch vss vss vdd vdd latch_n sky130_fd_sc_hd__inv_1
XM27 vss ibn_1u vss vss sky130_fd_pr__nfet_01v8 L=20 W=3 nf=1 ad='int((nf+1)/2) * W/nf * 0.29' as='int((nf+2)/2) * W/nf * 0.29'
+ pd='2*int((nf+1)/2) * (W/nf + 0.29)' ps='2*int((nf+2)/2) * (W/nf + 0.29)' nrd='0.29 / W' nrs='0.29 / W'
+ sa=0 sb=0 sd=0 mult=2 m=2
XM28 vss vss vss vss sky130_fd_pr__nfet_01v8_lvt L=1 W=2 nf=1 ad='int((nf+1)/2) * W/nf * 0.29' as='int((nf+2)/2) * W/nf * 0.29'
+ pd='2*int((nf+1)/2) * (W/nf + 0.29)' ps='2*int((nf+2)/2) * (W/nf + 0.29)' nrd='0.29 / W' nrs='0.29 / W'
+ sa=0 sb=0 sd=0 mult=2 m=2
XM29 vss vss vss vss sky130_fd_pr__nfet_01v8_lvt L=1 W=1 nf=1 ad='int((nf+1)/2) * W/nf * 0.29' as='int((nf+2)/2) * W/nf * 0.29'
+ pd='2*int((nf+1)/2) * (W/nf + 0.29)' ps='2*int((nf+2)/2) * (W/nf + 0.29)' nrd='0.29 / W' nrs='0.29 / W'
+ sa=0 sb=0 sd=0 mult=20 m=20
XM30 vdd vbp vdd vdd sky130_fd_pr__pfet_01v8_lvt L=5 W=5 nf=1 ad='int((nf+1)/2) * W/nf * 0.29' as='int((nf+2)/2) * W/nf * 0.29'
+ pd='2*int((nf+1)/2) * (W/nf + 0.29)' ps='2*int((nf+2)/2) * (W/nf + 0.29)' nrd='0.29 / W' nrs='0.29 / W'
+ sa=0 sb=0 sd=0 mult=2 m=2
XM31 vdd vdd vdd vdd sky130_fd_pr__pfet_01v8_lvt L=1 W=5 nf=1 ad='int((nf+1)/2) * W/nf * 0.29' as='int((nf+2)/2) * W/nf * 0.29'
+ pd='2*int((nf+1)/2) * (W/nf + 0.29)' ps='2*int((nf+2)/2) * (W/nf + 0.29)' nrd='0.29 / W' nrs='0.29 / W'
+ sa=0 sb=0 sd=0 mult=2 m=2
.ends

.GLOBAL GND
.end
